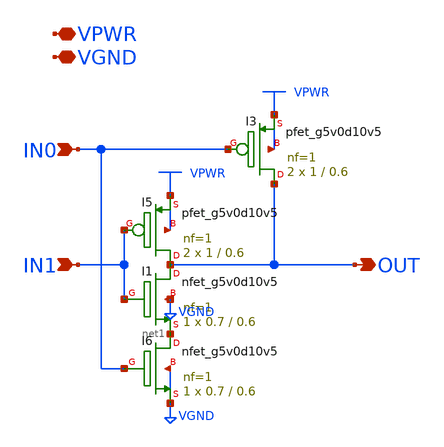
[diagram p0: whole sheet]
** sch_path: common/hvsbt_nand2.sch
* Copyright 2023 David Mitchell Bailey
* Licensed under the Apache License, Version 2.0 (the "License");
* you may not use this file except in compliance with the License.
* You may obtain a copy of the License at
* https://www.apache.org/licenses/LICENSE-2.0
* Unless required by applicable law or agreed to in writing, software
* distributed under the License is distributed on an "AS IS" BASIS,
* WITHOUT WARRANTIES OR CONDITIONS OF ANY KIND, either express or implied.
* See the License for the specific language governing permissions and
* limitations under the License.
**.subckt hvsbt_nand2 IN1 OUT VPWR VGND IN0
*.ipin IN1
*.opin OUT
*.iopin VPWR
*.iopin VGND
*.ipin IN0
XI1 OUT IN1 net1 VGND sky130_fd_pr__nfet_g5v0d10v5 L=0.6 W=0.7 nf=1 ad='int((nf+1)/2) * W/nf * 0.29'
+ as='int((nf+2)/2) * W/nf * 0.29' pd='2*int((nf+1)/2) * (W/nf + 0.29)' ps='2*int((nf+2)/2) * (W/nf + 0.29)'
+ nrd='0.29 / W' nrs='0.29 / W' sa=0 sb=0 sd=0 mult=1 m=1
XI5 OUT IN1 VPWR VPWR sky130_fd_pr__pfet_g5v0d10v5 L=0.6 W=1 nf=1 ad='int((nf+1)/2) * W/nf * 0.29' as='int((nf+2)/2) * W/nf * 0.29'
+ pd='2*int((nf+1)/2) * (W/nf + 0.29)' ps='2*int((nf+2)/2) * (W/nf + 0.29)' nrd='0.29 / W' nrs='0.29 / W'
+ sa=0 sb=0 sd=0 mult=2 m=2
XI3 OUT IN0 VPWR VPWR sky130_fd_pr__pfet_g5v0d10v5 L=0.6 W=1 nf=1 ad='int((nf+1)/2) * W/nf * 0.29' as='int((nf+2)/2) * W/nf * 0.29'
+ pd='2*int((nf+1)/2) * (W/nf + 0.29)' ps='2*int((nf+2)/2) * (W/nf + 0.29)' nrd='0.29 / W' nrs='0.29 / W'
+ sa=0 sb=0 sd=0 mult=2 m=2
XI6 net1 IN0 VGND VGND sky130_fd_pr__nfet_g5v0d10v5 L=0.6 W=0.7 nf=1 ad='int((nf+1)/2) * W/nf * 0.29'
+ as='int((nf+2)/2) * W/nf * 0.29' pd='2*int((nf+1)/2) * (W/nf + 0.29)' ps='2*int((nf+2)/2) * (W/nf + 0.29)'
+ nrd='0.29 / W' nrs='0.29 / W' sa=0 sb=0 sd=0 mult=1 m=1
**.ends
.end
